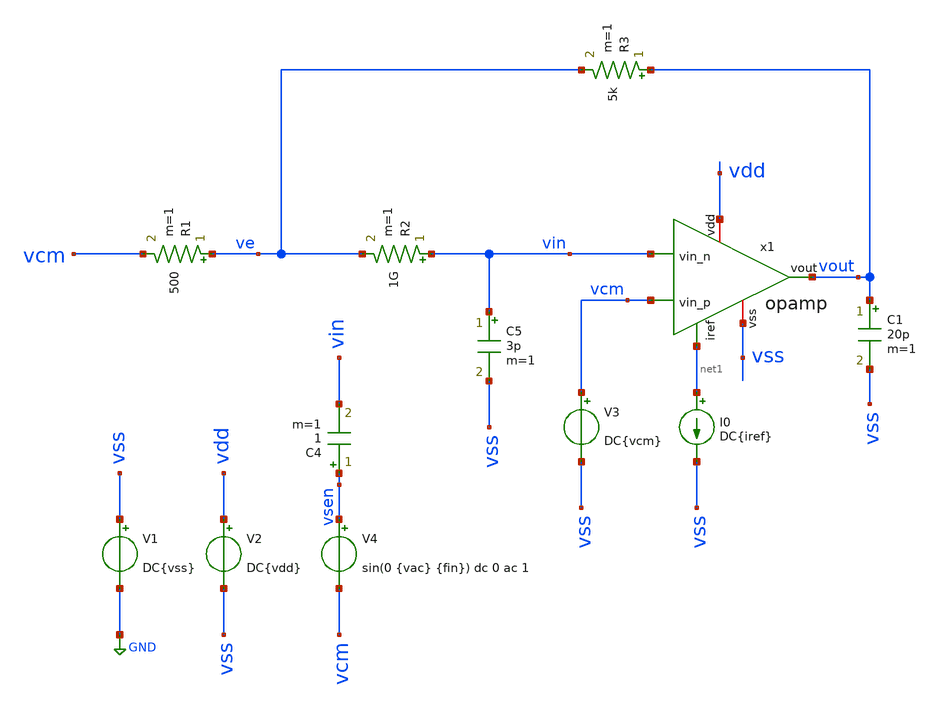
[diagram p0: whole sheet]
** sch_path: TpFinal/Mis Simulaciones/tb_opamp_openloop.sch
**.subckt tb_opamp_openloop
V1 vss GND DC{vss}
V2 vdd vss DC{vdd}
V3 vcm vss DC{vcm}
V4 vsen vcm sin(0 {vac} {fin}) dc 0 ac 1
C4 vsen vin 1 m=1
I0 net1 vss DC{iref}
R1 ve vcm 500 m=1
R2 vin ve 1G m=1
R3 vout ve 5k m=1
C5 vin vss 3p m=1
C1 vout vss 20p m=1
x1 vdd net1 vin vcm vout vss opamp
**** begin user architecture code




* Circuit Parameters
.param iref = 100u
.param vdd  = 1.8
.param vss  = 0.0
.param vcm  = 0.8
.param vac  = 10m
.param fin  = 9.765625e5
.options TEMP = 65.0

* Include Models
.lib ~/skywater/skywater-pdk/libraries/sky130_fd_pr_ngspice/latest/models/corners/sky130.lib TT

* OP Parameters & Singals to save
.save all  @M.X1.XM1.msky130_fd_pr__pfet_01v8_lvt[id] @M.X1.XM1.msky130_fd_pr__pfet_01v8_lvt[vth] @M.X1.XM1.msky130_fd_pr__pfet_01v8_lvt[vgs] @M.X1.XM1.msky130_fd_pr__pfet_01v8_lvt[vds] @M.X1.XM1.msky130_fd_pr__pfet_01v8_lvt[vdsat] @M.X1.XM1.msky130_fd_pr__pfet_01v8_lvt[gm] @M.X1.XM1.msky130_fd_pr__pfet_01v8_lvt[gds] @M.X1.XM1.msky130_fd_pr__pfet_01v8_lvt[cgg]  @M.X1.XM2.msky130_fd_pr__pfet_01v8_lvt[id] @M.X1.XM2.msky130_fd_pr__pfet_01v8_lvt[vth] @M.X1.XM2.msky130_fd_pr__pfet_01v8_lvt[vgs] @M.X1.XM2.msky130_fd_pr__pfet_01v8_lvt[vds] @M.X1.XM2.msky130_fd_pr__pfet_01v8_lvt[vdsat] @M.X1.XM2.msky130_fd_pr__pfet_01v8_lvt[gm] @M.X1.XM2.msky130_fd_pr__pfet_01v8_lvt[gds] @M.X1.XM2.msky130_fd_pr__pfet_01v8_lvt[cgg]  @M.X1.XM3.msky130_fd_pr__nfet_01v8[id] @M.X1.XM3.msky130_fd_pr__nfet_01v8[vth] @M.X1.XM3.msky130_fd_pr__nfet_01v8[vgs] @M.X1.XM3.msky130_fd_pr__nfet_01v8[vds] @M.X1.XM3.msky130_fd_pr__nfet_01v8[vdsat] @M.X1.XM3.msky130_fd_pr__nfet_01v8[gm] @M.X1.XM3.msky130_fd_pr__nfet_01v8[gds] @M.X1.XM3.msky130_fd_pr__nfet_01v8[cgg]  @M.X1.XM4.msky130_fd_pr__nfet_01v8[id] @M.X1.XM4.msky130_fd_pr__nfet_01v8[vth] @M.X1.XM4.msky130_fd_pr__nfet_01v8[vgs] @M.X1.XM4.msky130_fd_pr__nfet_01v8[vds] @M.X1.XM4.msky130_fd_pr__nfet_01v8[vdsat] @M.X1.XM4.msky130_fd_pr__nfet_01v8[gm] @M.X1.XM4.msky130_fd_pr__nfet_01v8[gds] @M.X1.XM4.msky130_fd_pr__nfet_01v8[cgg]  @M.X1.XM5.msky130_fd_pr__pfet_01v8[id] @M.X1.XM5.msky130_fd_pr__pfet_01v8[vth] @M.X1.XM5.msky130_fd_pr__pfet_01v8[vgs] @M.X1.XM5.msky130_fd_pr__pfet_01v8[vds] @M.X1.XM5.msky130_fd_pr__pfet_01v8[vdsat] @M.X1.XM5.msky130_fd_pr__pfet_01v8[gm] @M.X1.XM5.msky130_fd_pr__pfet_01v8[gds] @M.X1.XM5.msky130_fd_pr__pfet_01v8[cgg]  @M.X1.XM6.msky130_fd_pr__nfet_01v8[id] @M.X1.XM6.msky130_fd_pr__nfet_01v8[vth] @M.X1.XM6.msky130_fd_pr__nfet_01v8[vgs] @M.X1.XM6.msky130_fd_pr__nfet_01v8[vds] @M.X1.XM6.msky130_fd_pr__nfet_01v8[vdsat] @M.X1.XM6.msky130_fd_pr__nfet_01v8[gm] @M.X1.XM6.msky130_fd_pr__nfet_01v8[gds] @M.X1.XM6.msky130_fd_pr__nfet_01v8[cgg]  @M.X1.XM7.msky130_fd_pr__pfet_01v8[id] @M.X1.XM7.msky130_fd_pr__pfet_01v8[vth] @M.X1.XM7.msky130_fd_pr__pfet_01v8[vgs] @M.X1.XM7.msky130_fd_pr__pfet_01v8[vds] @M.X1.XM7.msky130_fd_pr__pfet_01v8[vdsat] @M.X1.XM7.msky130_fd_pr__pfet_01v8[gm] @M.X1.XM7.msky130_fd_pr__pfet_01v8[gds] @M.X1.XM7.msky130_fd_pr__pfet_01v8[cgg]  @M.X1.XM8.msky130_fd_pr__pfet_01v8[id] @M.X1.XM8.msky130_fd_pr__pfet_01v8[vth] @M.X1.XM8.msky130_fd_pr__pfet_01v8[vgs] @M.X1.XM8.msky130_fd_pr__pfet_01v8[vds] @M.X1.XM8.msky130_fd_pr__pfet_01v8[vdsat] @M.X1.XM8.msky130_fd_pr__pfet_01v8[gm] @M.X1.XM8.msky130_fd_pr__pfet_01v8[gds] @M.X1.XM8.msky130_fd_pr__pfet_01v8[cgg]  @M.X1.XM9.msky130_fd_pr__nfet_01v8[id] @M.X1.XM9.msky130_fd_pr__nfet_01v8[vth] @M.X1.XM9.msky130_fd_pr__nfet_01v8[vgs] @M.X1.XM9.msky130_fd_pr__nfet_01v8[vds] @M.X1.XM9.msky130_fd_pr__nfet_01v8[vdsat] @M.X1.XM9.msky130_fd_pr__nfet_01v8[gm] @M.X1.XM9.msky130_fd_pr__nfet_01v8[gds] @M.X1.XM9.msky130_fd_pr__nfet_01v8[cgg]

*Simulation
.control
  set color0 = white

  ac dec 100 1 10G
  setplot ac1
  meas ac GBW when vdb(vout)=0
  meas ac DCG find vdb(vout) at=1
  meas ac PM find vp(vout) when vdb(vout)=0
  print PM*180/PI
  meas ac GM find vdb(vout) when vp(vout)=0
  plot vdb(vout) {vp(vout)*180/PI}
  write tb_opamp_openloop_ac1.raw

  reset
  op
  setplot op1
  unset filetype
  write tb_opamp_openloop.raw
.endc

.end


**** end user architecture code
**.ends

* expanding   symbol:  opamp.sym # of pins=6
** sym_path: opamp.sym
** sch_path: opamp.sch
.subckt opamp vdd iref vin_n vin_p vout vss
*.iopin vdd
*.iopin vss
*.ipin vin_n
*.ipin vin_p
*.ipin iref
*.opin vout
XM3 vbn vbn vss vss sky130_fd_pr__nfet_01v8 L=3.6 W=40 nf=1 ad='W * 0.29' as='W * 0.29' pd='2 * (W + 0.29)'
+ ps='2 * (W + 0.29)' nrd='0.29 / W' nrs='0.29 / W' sa=0 sb=0 sd=0 mult=17 m=17
XM4 voe1 vbn vss vss sky130_fd_pr__nfet_01v8 L=3.6 W=40 nf=1 ad='W * 0.29' as='W * 0.29' pd='2 * (W + 0.29)'
+ ps='2 * (W + 0.29)' nrd='0.29 / W' nrs='0.29 / W' sa=0 sb=0 sd=0 mult=17 m=17
XM5 vp iref vdd vdd sky130_fd_pr__pfet_01v8 L=0.8 W=60 nf=1 ad='W * 0.29' as='W * 0.29' pd='2 * (W + 0.29)'
+ ps='2 * (W + 0.29)' nrd='0.29 / W' nrs='0.29 / W' sa=0 sb=0 sd=0 mult=54 m=54
XM7 vout iref vdd vdd sky130_fd_pr__pfet_01v8 L=0.8 W=60 nf=1 ad='W * 0.29' as='W * 0.29' pd='2 * (W + 0.29)'
+ ps='2 * (W + 0.29)' nrd='0.29 / W' nrs='0.29 / W' sa=0 sb=0 sd=0 mult=68 m=68
XM8 iref iref vdd vdd sky130_fd_pr__pfet_01v8 L=0.8 W=60 nf=1 ad='W * 0.29' as='W * 0.29' pd='2 * (W + 0.29)'
+ ps='2 * (W + 0.29)' nrd='0.29 / W' nrs='0.29 / W' sa=0 sb=0 sd=0 mult=5 m=5
XM9 net1 vdd voe1 vss sky130_fd_pr__nfet_01v8 L=0.15 W=8.1 nf=1 ad='W * 0.29' as='W * 0.29' pd='2 * (W + 0.29)'
+ ps='2 * (W + 0.29)' nrd='0.29 / W' nrs='0.29 / W' sa=0 sb=0 sd=0 mult=1 m=1
XM6 vout voe1 vss vss sky130_fd_pr__nfet_01v8 L=0.16 W=82 nf=1 ad='W * 0.29' as='W * 0.29' pd='2 * (W + 0.29)'
+ ps='2 * (W + 0.29)' nrd='0.29 / W' nrs='0.29 / W' sa=0 sb=0 sd=0 mult=14 m=14
XM1 vbn vin_n vp vp sky130_fd_pr__pfet_01v8_lvt L=0.5 W=45 nf=1 ad='int((nf+1)/2) * W/nf * 0.29' as='int((nf+2)/2) * W/nf * 0.29'
+ pd='2*int((nf+1)/2) * (W/nf + 0.29)' ps='2*int((nf+2)/2) * (W/nf + 0.29)' nrd='0.29 / W' nrs='0.29 / W'
+ sa=0 sb=0 sd=0 mult=20 m=20
XM2 voe1 vin_p vp vp sky130_fd_pr__pfet_01v8_lvt L=0.5 W=45 nf=1 ad='int((nf+1)/2) * W/nf * 0.29' as='int((nf+2)/2) * W/nf * 0.29'
+ pd='2*int((nf+1)/2) * (W/nf + 0.29)' ps='2*int((nf+2)/2) * (W/nf + 0.29)' nrd='0.29 / W' nrs='0.29 / W'
+ sa=0 sb=0 sd=0 mult=20 m=20
C1 net1 vout 9.5p m=1
.ends

.GLOBAL GND
.end
